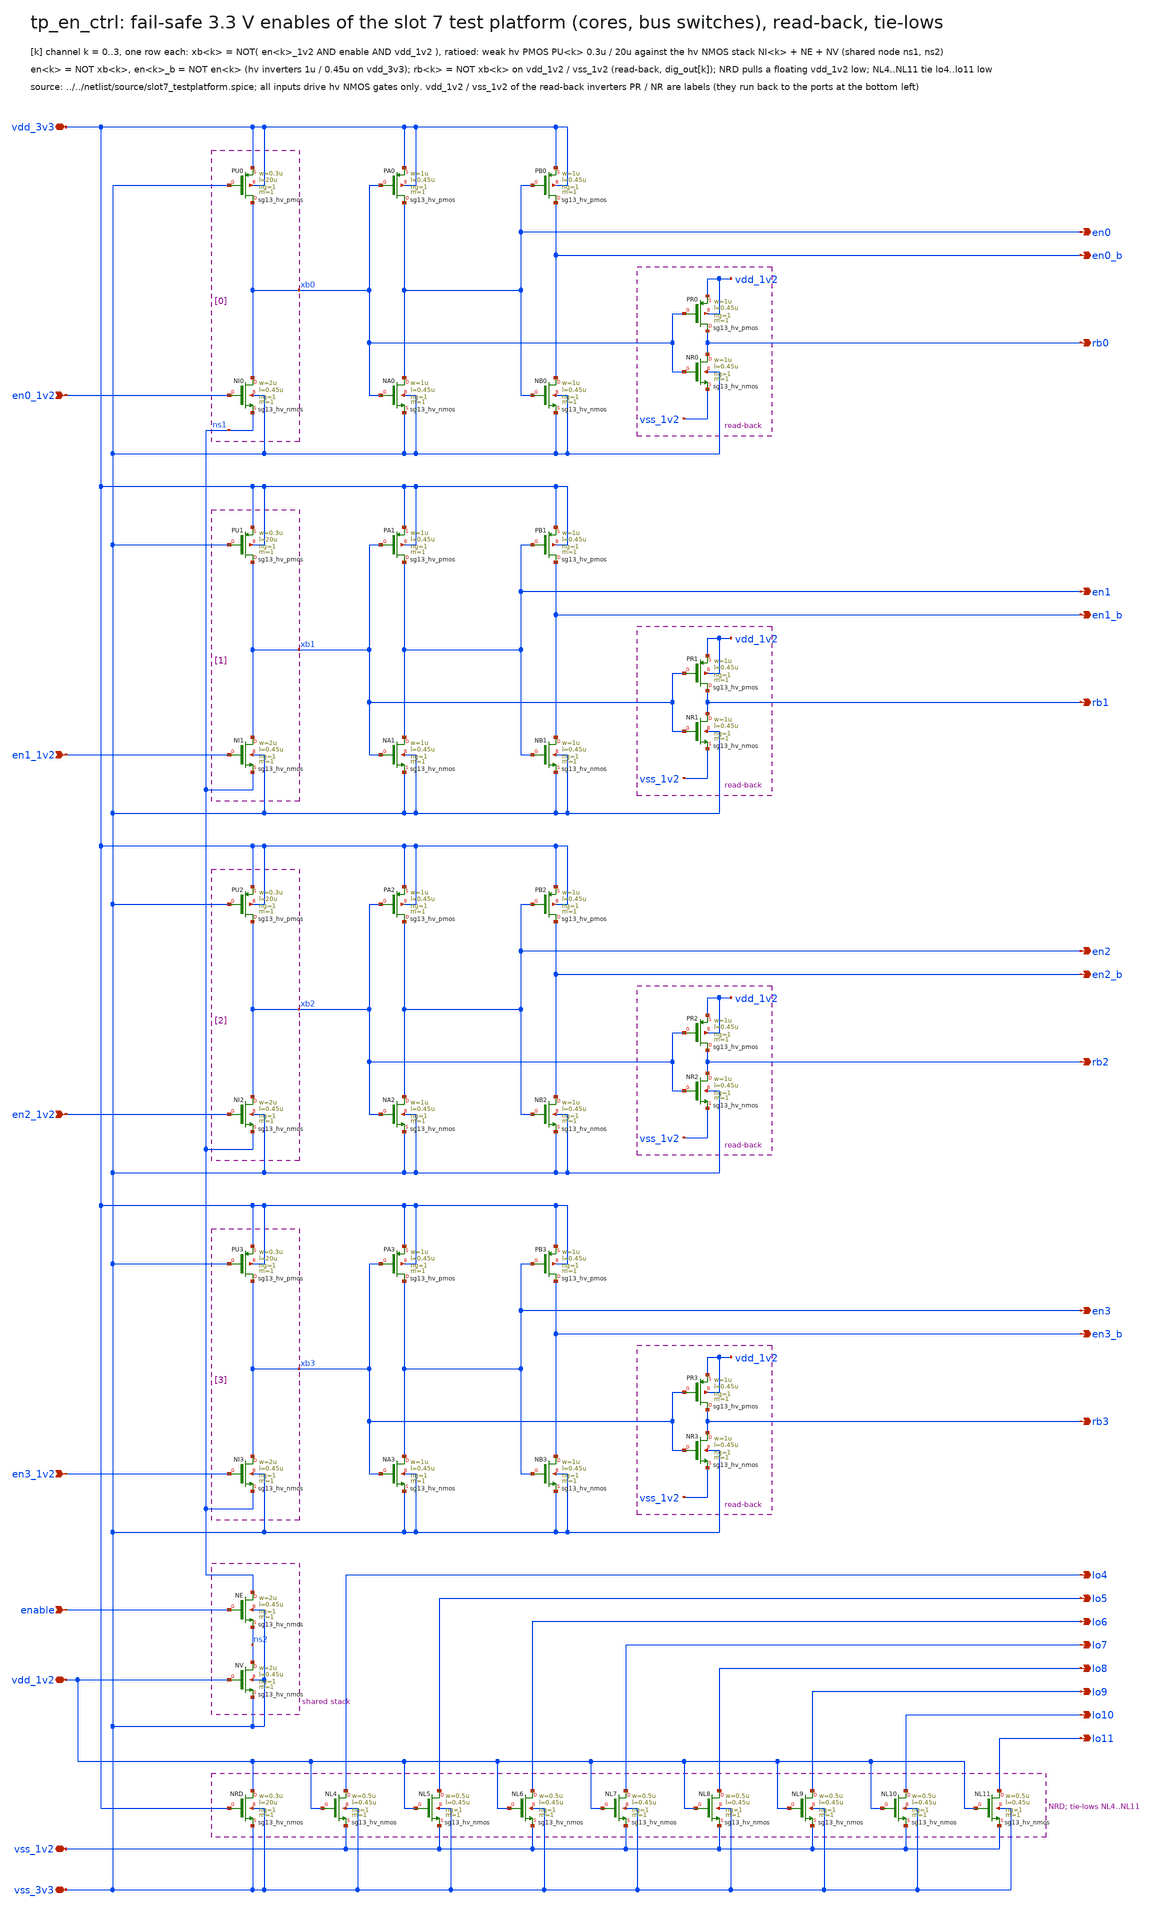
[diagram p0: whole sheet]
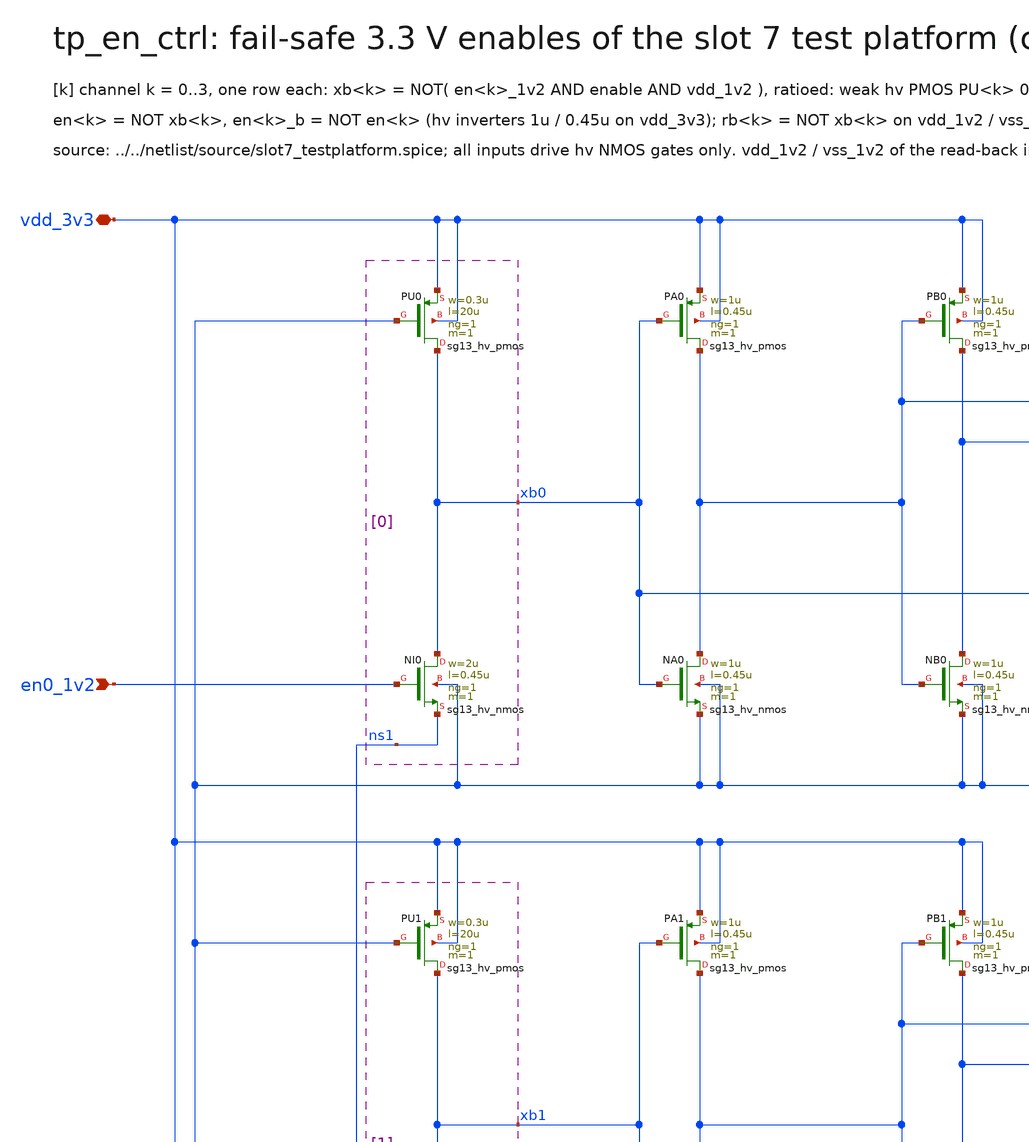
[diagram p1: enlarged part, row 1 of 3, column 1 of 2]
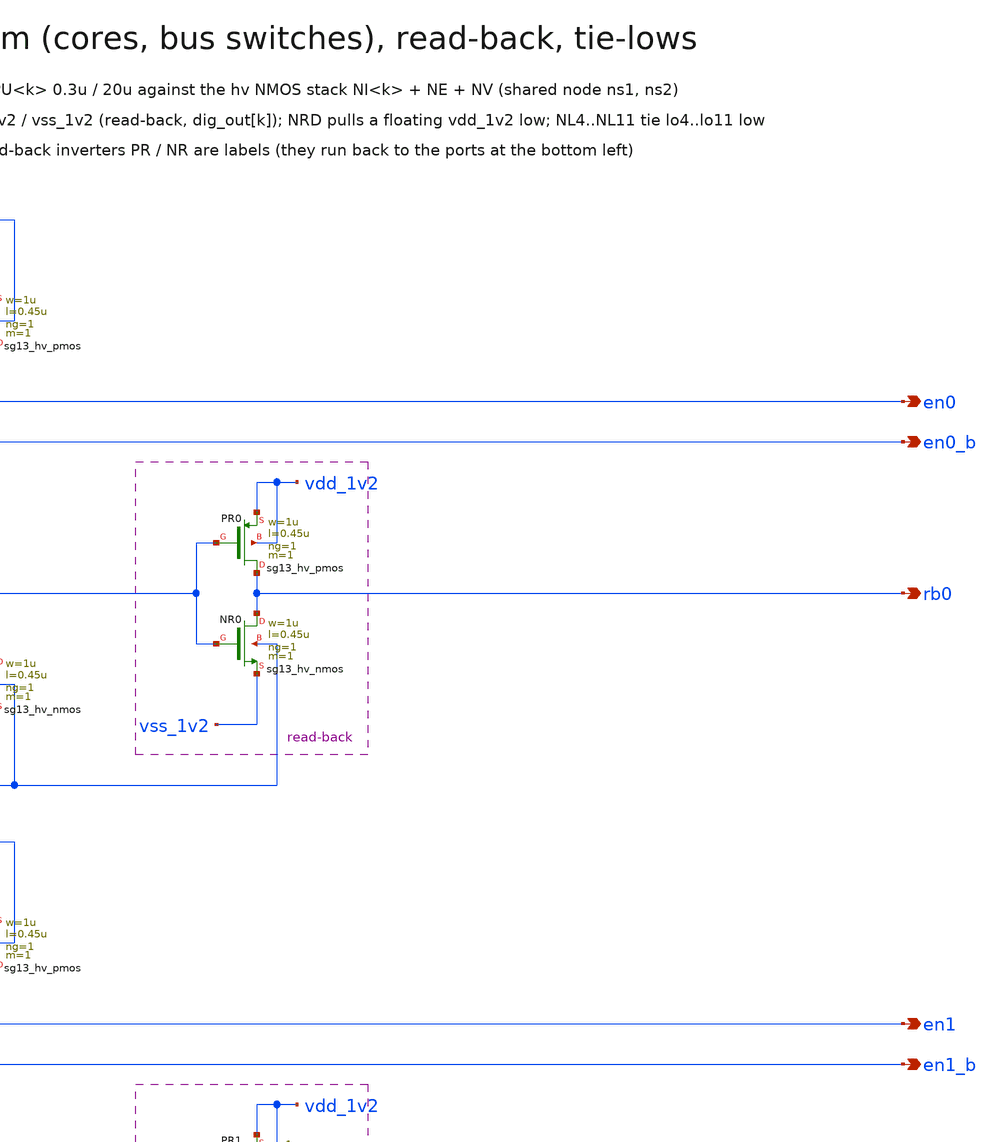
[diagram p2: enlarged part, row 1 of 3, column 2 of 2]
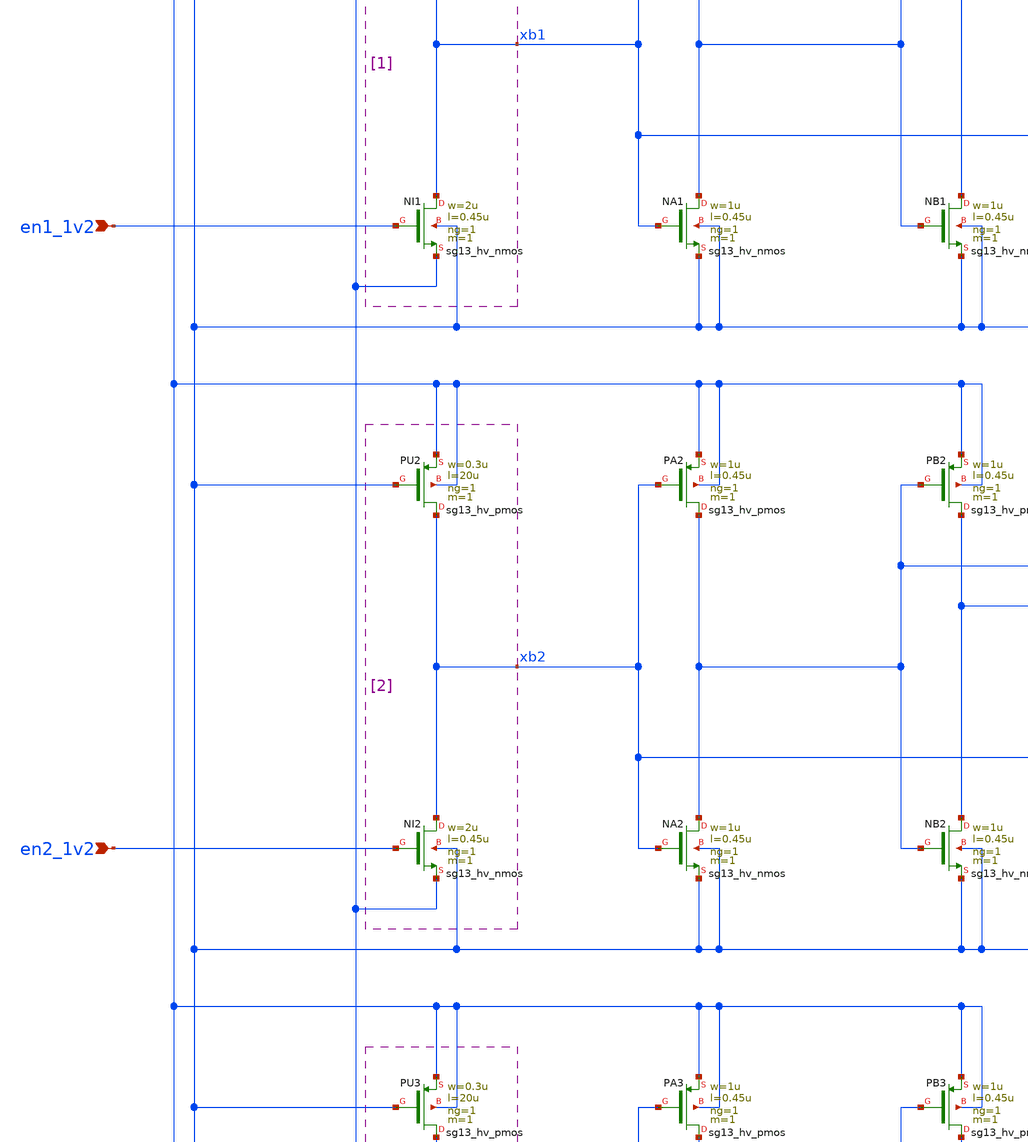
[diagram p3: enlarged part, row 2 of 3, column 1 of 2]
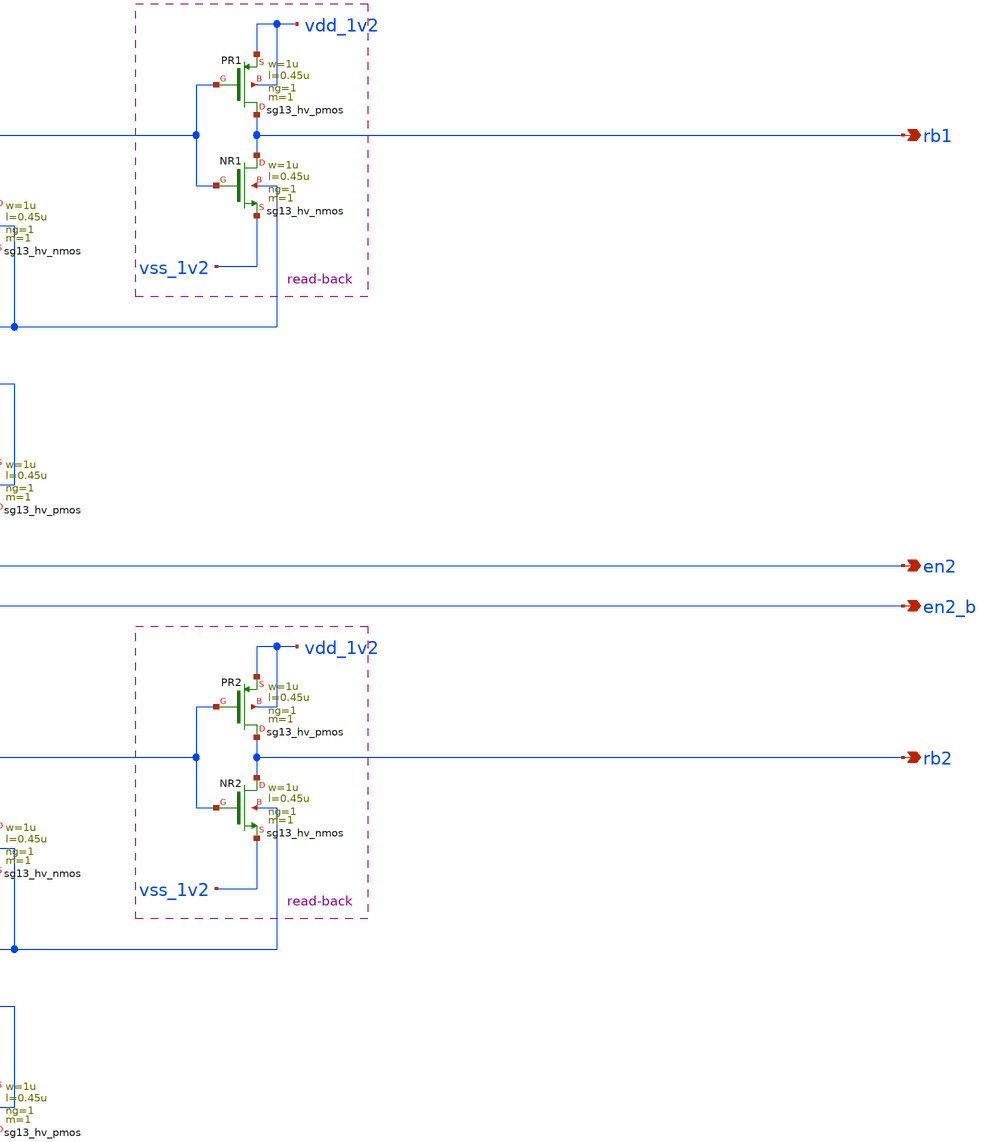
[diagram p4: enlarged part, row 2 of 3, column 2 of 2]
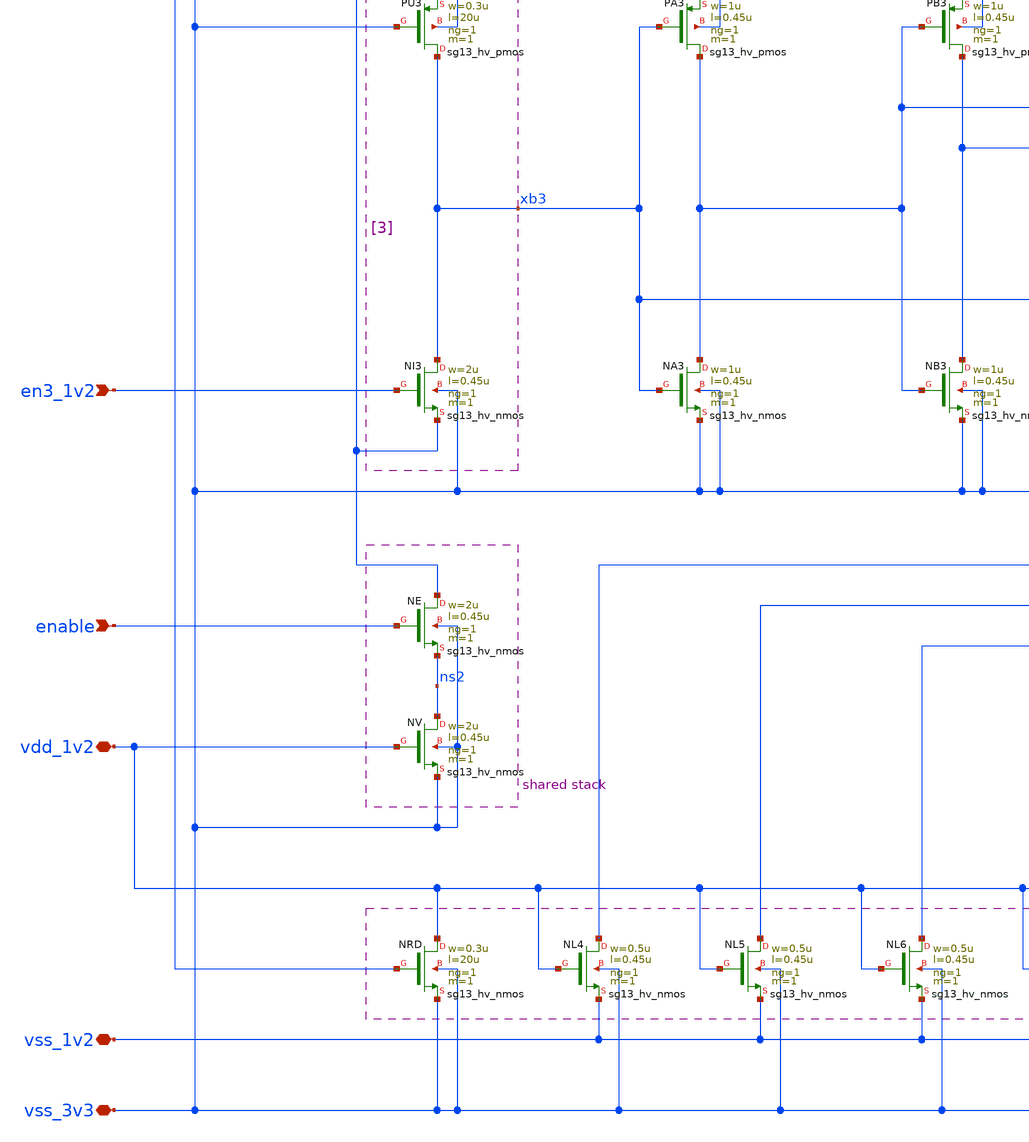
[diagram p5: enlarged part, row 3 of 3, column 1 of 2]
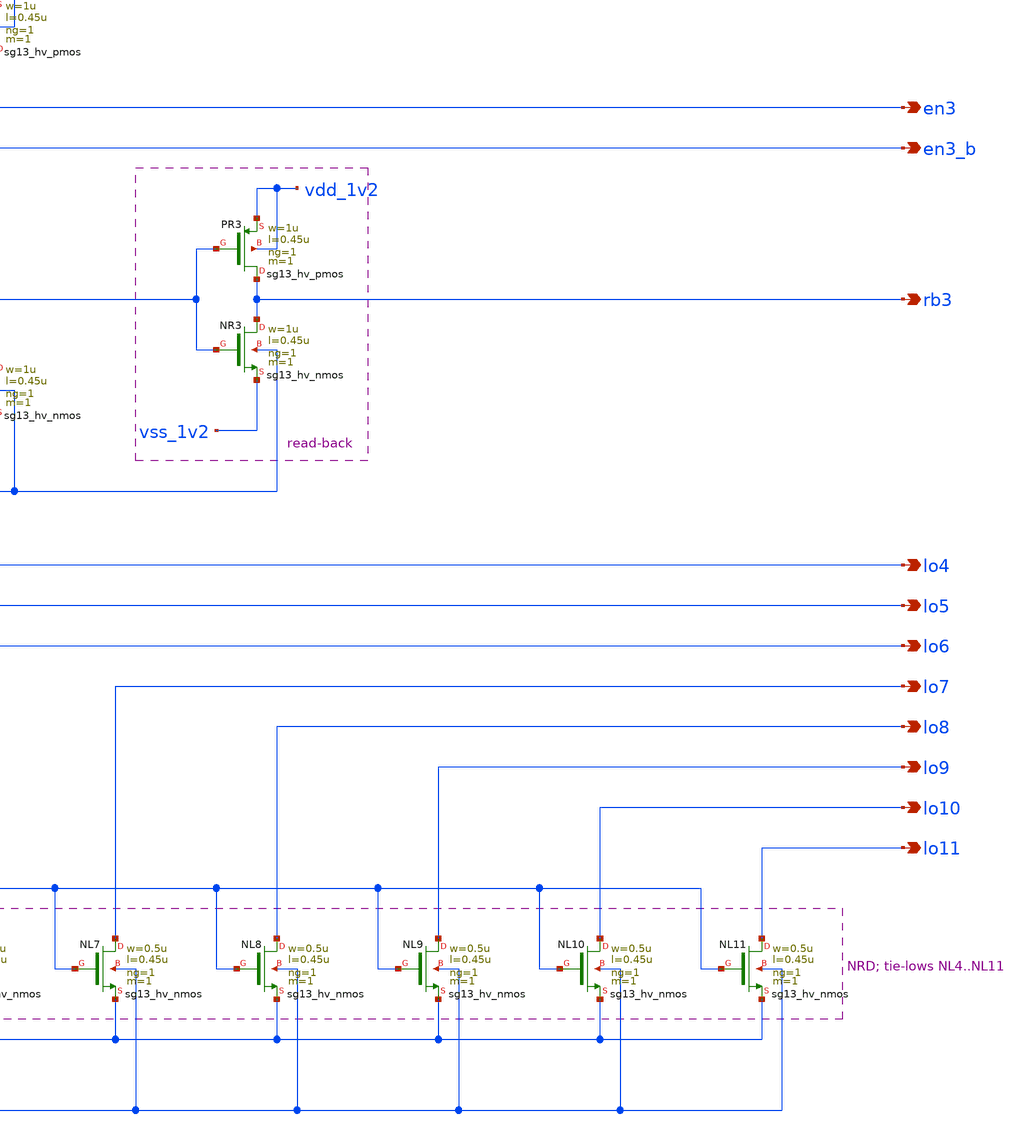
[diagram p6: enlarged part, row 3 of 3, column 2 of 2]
** sch_path: macros/slot7_testplatform/schematic/xschem_drawn/tp_en_ctrl.sch
**.subckt tp_en_ctrl vdd_3v3 vss_3v3 vdd_1v2 vss_1v2 en0_1v2 en1_1v2 en2_1v2 en3_1v2 enable en0
*+ en0_b en1 en1_b en2 en2_b en3 en3_b rb0 rb1 rb2 rb3 lo4 lo5 lo6 lo7 lo8 lo9 lo10 lo11
*.iopin vdd_3v3
*.iopin vss_3v3
*.iopin vdd_1v2
*.iopin vss_1v2
*.ipin en0_1v2
*.ipin en1_1v2
*.ipin en2_1v2
*.ipin en3_1v2
*.ipin enable
*.opin en0
*.opin en0_b
*.opin en1
*.opin en1_b
*.opin en2
*.opin en2_b
*.opin en3
*.opin en3_b
*.opin rb0
*.opin rb1
*.opin rb2
*.opin rb3
*.opin lo4
*.opin lo5
*.opin lo6
*.opin lo7
*.opin lo8
*.opin lo9
*.opin lo10
*.opin lo11
XPU0 xb0 vss_3v3 vdd_3v3 vdd_3v3 sg13_hv_pmos w=0.3u l=20u ng=1 m=1 mm_ok=1
XNI0 xb0 en0_1v2 ns1 vss_3v3 sg13_hv_nmos w=2u l=0.45u ng=1 m=1 mm_ok=1
XPA0 en0 xb0 vdd_3v3 vdd_3v3 sg13_hv_pmos w=1u l=0.45u ng=1 m=1 mm_ok=1
XNA0 en0 xb0 vss_3v3 vss_3v3 sg13_hv_nmos w=1u l=0.45u ng=1 m=1 mm_ok=1
XPB0 en0_b en0 vdd_3v3 vdd_3v3 sg13_hv_pmos w=1u l=0.45u ng=1 m=1 mm_ok=1
XNB0 en0_b en0 vss_3v3 vss_3v3 sg13_hv_nmos w=1u l=0.45u ng=1 m=1 mm_ok=1
XPR0 rb0 xb0 vdd_1v2 vdd_1v2 sg13_hv_pmos w=1u l=0.45u ng=1 m=1 mm_ok=1
XNR0 rb0 xb0 vss_1v2 vss_3v3 sg13_hv_nmos w=1u l=0.45u ng=1 m=1 mm_ok=1
XPU1 xb1 vss_3v3 vdd_3v3 vdd_3v3 sg13_hv_pmos w=0.3u l=20u ng=1 m=1 mm_ok=1
XNI1 xb1 en1_1v2 ns1 vss_3v3 sg13_hv_nmos w=2u l=0.45u ng=1 m=1 mm_ok=1
XPA1 en1 xb1 vdd_3v3 vdd_3v3 sg13_hv_pmos w=1u l=0.45u ng=1 m=1 mm_ok=1
XNA1 en1 xb1 vss_3v3 vss_3v3 sg13_hv_nmos w=1u l=0.45u ng=1 m=1 mm_ok=1
XPB1 en1_b en1 vdd_3v3 vdd_3v3 sg13_hv_pmos w=1u l=0.45u ng=1 m=1 mm_ok=1
XNB1 en1_b en1 vss_3v3 vss_3v3 sg13_hv_nmos w=1u l=0.45u ng=1 m=1 mm_ok=1
XPR1 rb1 xb1 vdd_1v2 vdd_1v2 sg13_hv_pmos w=1u l=0.45u ng=1 m=1 mm_ok=1
XNR1 rb1 xb1 vss_1v2 vss_3v3 sg13_hv_nmos w=1u l=0.45u ng=1 m=1 mm_ok=1
XPU2 xb2 vss_3v3 vdd_3v3 vdd_3v3 sg13_hv_pmos w=0.3u l=20u ng=1 m=1 mm_ok=1
XNI2 xb2 en2_1v2 ns1 vss_3v3 sg13_hv_nmos w=2u l=0.45u ng=1 m=1 mm_ok=1
XPA2 en2 xb2 vdd_3v3 vdd_3v3 sg13_hv_pmos w=1u l=0.45u ng=1 m=1 mm_ok=1
XNA2 en2 xb2 vss_3v3 vss_3v3 sg13_hv_nmos w=1u l=0.45u ng=1 m=1 mm_ok=1
XPB2 en2_b en2 vdd_3v3 vdd_3v3 sg13_hv_pmos w=1u l=0.45u ng=1 m=1 mm_ok=1
XNB2 en2_b en2 vss_3v3 vss_3v3 sg13_hv_nmos w=1u l=0.45u ng=1 m=1 mm_ok=1
XPR2 rb2 xb2 vdd_1v2 vdd_1v2 sg13_hv_pmos w=1u l=0.45u ng=1 m=1 mm_ok=1
XNR2 rb2 xb2 vss_1v2 vss_3v3 sg13_hv_nmos w=1u l=0.45u ng=1 m=1 mm_ok=1
XPU3 xb3 vss_3v3 vdd_3v3 vdd_3v3 sg13_hv_pmos w=0.3u l=20u ng=1 m=1 mm_ok=1
XNI3 xb3 en3_1v2 ns1 vss_3v3 sg13_hv_nmos w=2u l=0.45u ng=1 m=1 mm_ok=1
XPA3 en3 xb3 vdd_3v3 vdd_3v3 sg13_hv_pmos w=1u l=0.45u ng=1 m=1 mm_ok=1
XNA3 en3 xb3 vss_3v3 vss_3v3 sg13_hv_nmos w=1u l=0.45u ng=1 m=1 mm_ok=1
XPB3 en3_b en3 vdd_3v3 vdd_3v3 sg13_hv_pmos w=1u l=0.45u ng=1 m=1 mm_ok=1
XNB3 en3_b en3 vss_3v3 vss_3v3 sg13_hv_nmos w=1u l=0.45u ng=1 m=1 mm_ok=1
XPR3 rb3 xb3 vdd_1v2 vdd_1v2 sg13_hv_pmos w=1u l=0.45u ng=1 m=1 mm_ok=1
XNR3 rb3 xb3 vss_1v2 vss_3v3 sg13_hv_nmos w=1u l=0.45u ng=1 m=1 mm_ok=1
XNE ns1 enable ns2 vss_3v3 sg13_hv_nmos w=2u l=0.45u ng=1 m=1 mm_ok=1
XNV ns2 vdd_1v2 vss_3v3 vss_3v3 sg13_hv_nmos w=2u l=0.45u ng=1 m=1 mm_ok=1
XNRD vdd_1v2 vdd_3v3 vss_3v3 vss_3v3 sg13_hv_nmos w=0.3u l=20u ng=1 m=1 mm_ok=1
XNL4 lo4 vdd_1v2 vss_1v2 vss_3v3 sg13_hv_nmos w=0.5u l=0.45u ng=1 m=1 mm_ok=1
XNL5 lo5 vdd_1v2 vss_1v2 vss_3v3 sg13_hv_nmos w=0.5u l=0.45u ng=1 m=1 mm_ok=1
XNL6 lo6 vdd_1v2 vss_1v2 vss_3v3 sg13_hv_nmos w=0.5u l=0.45u ng=1 m=1 mm_ok=1
XNL7 lo7 vdd_1v2 vss_1v2 vss_3v3 sg13_hv_nmos w=0.5u l=0.45u ng=1 m=1 mm_ok=1
XNL8 lo8 vdd_1v2 vss_1v2 vss_3v3 sg13_hv_nmos w=0.5u l=0.45u ng=1 m=1 mm_ok=1
XNL9 lo9 vdd_1v2 vss_1v2 vss_3v3 sg13_hv_nmos w=0.5u l=0.45u ng=1 m=1 mm_ok=1
XNL10 lo10 vdd_1v2 vss_1v2 vss_3v3 sg13_hv_nmos w=0.5u l=0.45u ng=1 m=1 mm_ok=1
XNL11 lo11 vdd_1v2 vss_1v2 vss_3v3 sg13_hv_nmos w=0.5u l=0.45u ng=1 m=1 mm_ok=1
**.ends
.end
